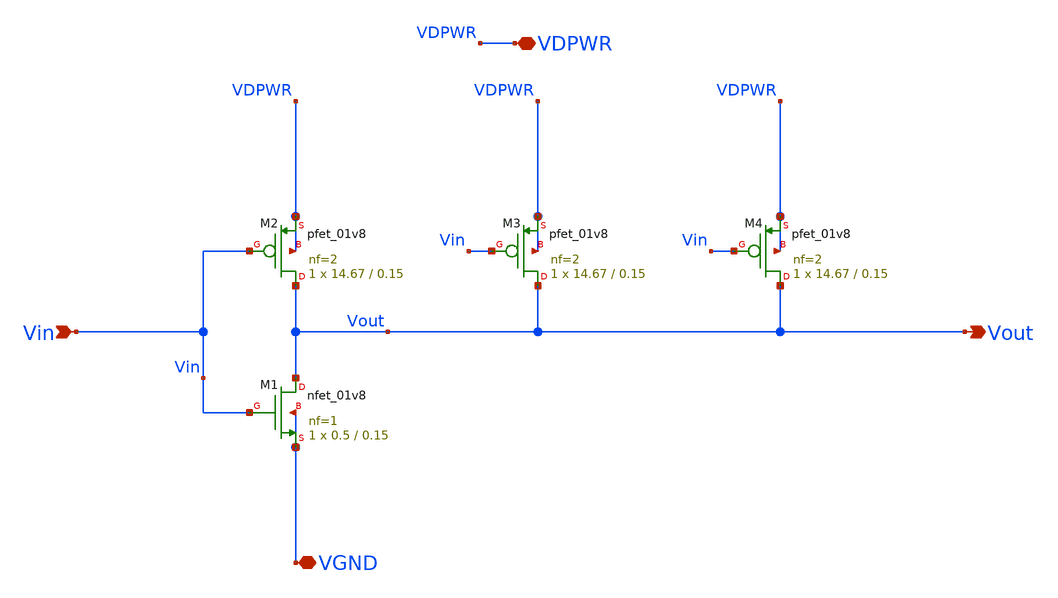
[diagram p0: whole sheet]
** sch_path: xschem/INVERTER_SIZES/inverter_p44_n0o5.sch
**.subckt inverter_p44_n0o5 Vout Vin VDPWR VGND
*.opin Vout
*.ipin Vin
*.iopin VDPWR
*.iopin VGND
XM1 Vout Vin VGND VGND sky130_fd_pr__nfet_01v8 L=0.15 W=0.5 nf=1 ad='int((nf+1)/2) * W/nf * 0.29' as='int((nf+2)/2) * W/nf * 0.29'
+ pd='2*int((nf+1)/2) * (W/nf + 0.29)' ps='2*int((nf+2)/2) * (W/nf + 0.29)' nrd='0.29 / W' nrs='0.29 / W'
+ sa=0 sb=0 sd=0 mult=1 m=1
XM2 Vout Vin VDPWR VDPWR sky130_fd_pr__pfet_01v8 L=0.15 W=14.67 nf=2 ad='int((nf+1)/2) * W/nf * 0.29'
+ as='int((nf+2)/2) * W/nf * 0.29' pd='2*int((nf+1)/2) * (W/nf + 0.29)' ps='2*int((nf+2)/2) * (W/nf + 0.29)'
+ nrd='0.29 / W' nrs='0.29 / W' sa=0 sb=0 sd=0 mult=1 m=1
XM3 Vout Vin VDPWR VDPWR sky130_fd_pr__pfet_01v8 L=0.15 W=14.67 nf=2 ad='int((nf+1)/2) * W/nf * 0.29'
+ as='int((nf+2)/2) * W/nf * 0.29' pd='2*int((nf+1)/2) * (W/nf + 0.29)' ps='2*int((nf+2)/2) * (W/nf + 0.29)'
+ nrd='0.29 / W' nrs='0.29 / W' sa=0 sb=0 sd=0 mult=1 m=1
XM4 Vout Vin VDPWR VDPWR sky130_fd_pr__pfet_01v8 L=0.15 W=14.67 nf=2 ad='int((nf+1)/2) * W/nf * 0.29'
+ as='int((nf+2)/2) * W/nf * 0.29' pd='2*int((nf+1)/2) * (W/nf + 0.29)' ps='2*int((nf+2)/2) * (W/nf + 0.29)'
+ nrd='0.29 / W' nrs='0.29 / W' sa=0 sb=0 sd=0 mult=1 m=1
**.ends
.end
